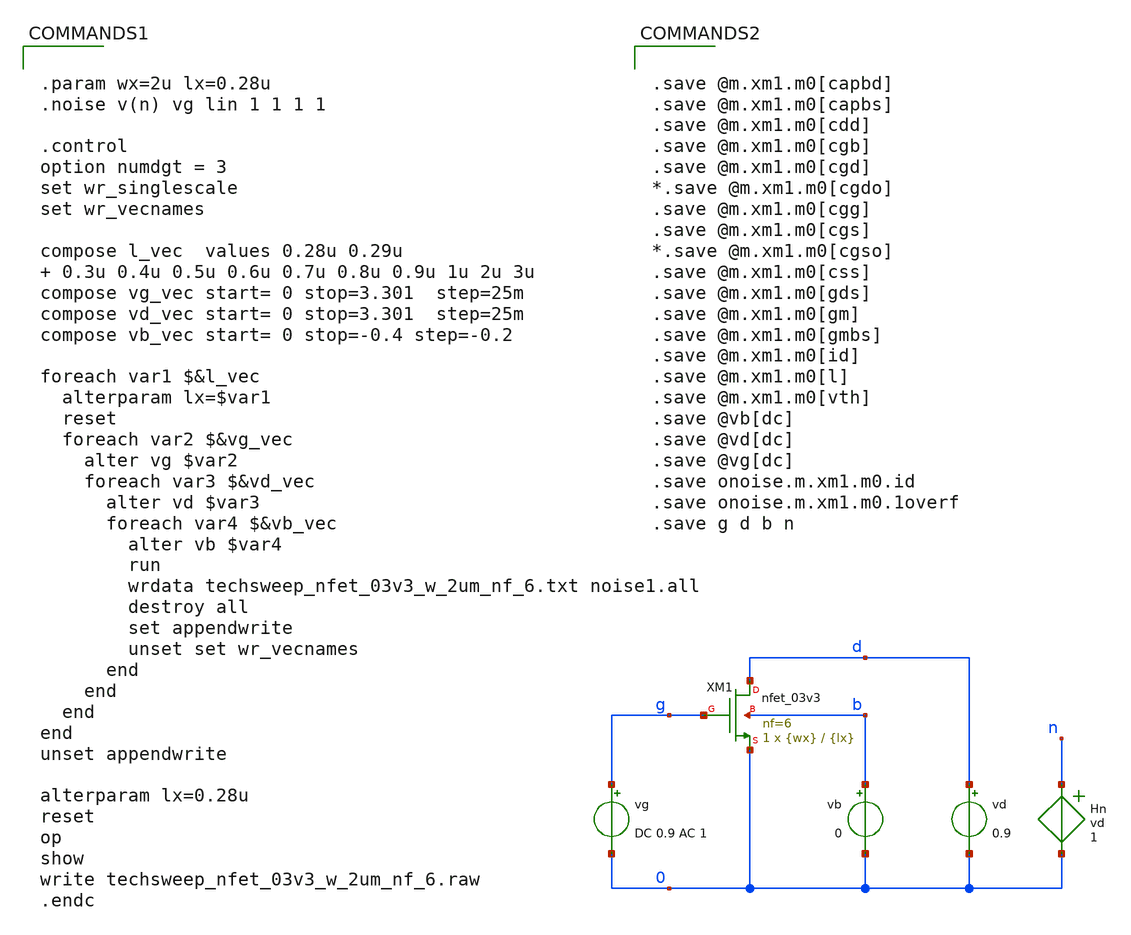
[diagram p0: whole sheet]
** sch_path: src/jupyter_notebooks/gmId/gm-ID-gf180mcuD/starter_files_open_source_tools/gf180mcuD/techsweep_nfet_03v3.sch
**.subckt techsweep_nfet_03v3
vg g 0 DC 0.9 AC 1
vd d 0 0.9
vb b 0 0
Hn n 0 vd 1
XM1 d g 0 b nfet_03v3 L={lx} W={wx} nf=6 ad='int((nf+1)/2) * W/nf * 0.18u' as='int((nf+2)/2) * W/nf * 0.18u'
+ pd='2*int((nf+1)/2) * (W/nf + 0.18u)' ps='2*int((nf+2)/2) * (W/nf + 0.18u)' nrd='0.18u / W' nrs='0.18u / W'
+ sa=0 sb=0 sd=0 m=1
**** begin user architecture code


.param wx=2u lx=0.28u
.noise v(n) vg lin 1 1 1 1

.control
option numdgt = 3
set wr_singlescale
set wr_vecnames

compose l_vec  values 0.28u 0.29u  0.3u 0.4u 0.5u 0.6u 0.7u 0.8u 0.9u 1u 2u 3u
compose vg_vec start= 0 stop=3.301  step=25m
compose vd_vec start= 0 stop=3.301  step=25m
compose vb_vec start= 0 stop=-0.4 step=-0.2

foreach var1 $&l_vec
  alterparam lx=$var1
  reset
  foreach var2 $&vg_vec
    alter vg $var2
    foreach var3 $&vd_vec
      alter vd $var3
      foreach var4 $&vb_vec
        alter vb $var4
        run
        wrdata techsweep_nfet_03v3_w_2um_nf_6.txt noise1.all
        destroy all
        set appendwrite
        unset set wr_vecnames
      end
    end
  end
end
unset appendwrite

alterparam lx=0.28u
reset
op
show
write techsweep_nfet_03v3_w_2um_nf_6.raw
.endc




.save @m.xm1.m0[capbd]
.save @m.xm1.m0[capbs]
.save @m.xm1.m0[cdd]
.save @m.xm1.m0[cgb]
.save @m.xm1.m0[cgd]
*.save @m.xm1.m0[cgdo]
.save @m.xm1.m0[cgg]
.save @m.xm1.m0[cgs]
*.save @m.xm1.m0[cgso]
.save @m.xm1.m0[css]
.save @m.xm1.m0[gds]
.save @m.xm1.m0[gm]
.save @m.xm1.m0[gmbs]
.save @m.xm1.m0[id]
.save @m.xm1.m0[l]
.save @m.xm1.m0[vth]
.save @vb[dc]
.save @vd[dc]
.save @vg[dc]
.save onoise.m.xm1.m0.id
.save onoise.m.xm1.m0.1overf
.save g d b n



.include /home/vasil/Downloads/SSCS_PICO_2025/src/jupyter_notebooks/gmId/gm-ID-gf180mcuD/starter_files_open_source_tools/gf180mcuD/models_updated_2025.07.19/ngspice/design.ngspice
.lib /home/vasil/Downloads/SSCS_PICO_2025/src/jupyter_notebooks/gmId/gm-ID-gf180mcuD/starter_files_open_source_tools/gf180mcuD/models_updated_2025.07.19/ngspice/sm141064.ngspice typical

**** end user architecture code
**.ends
.end
